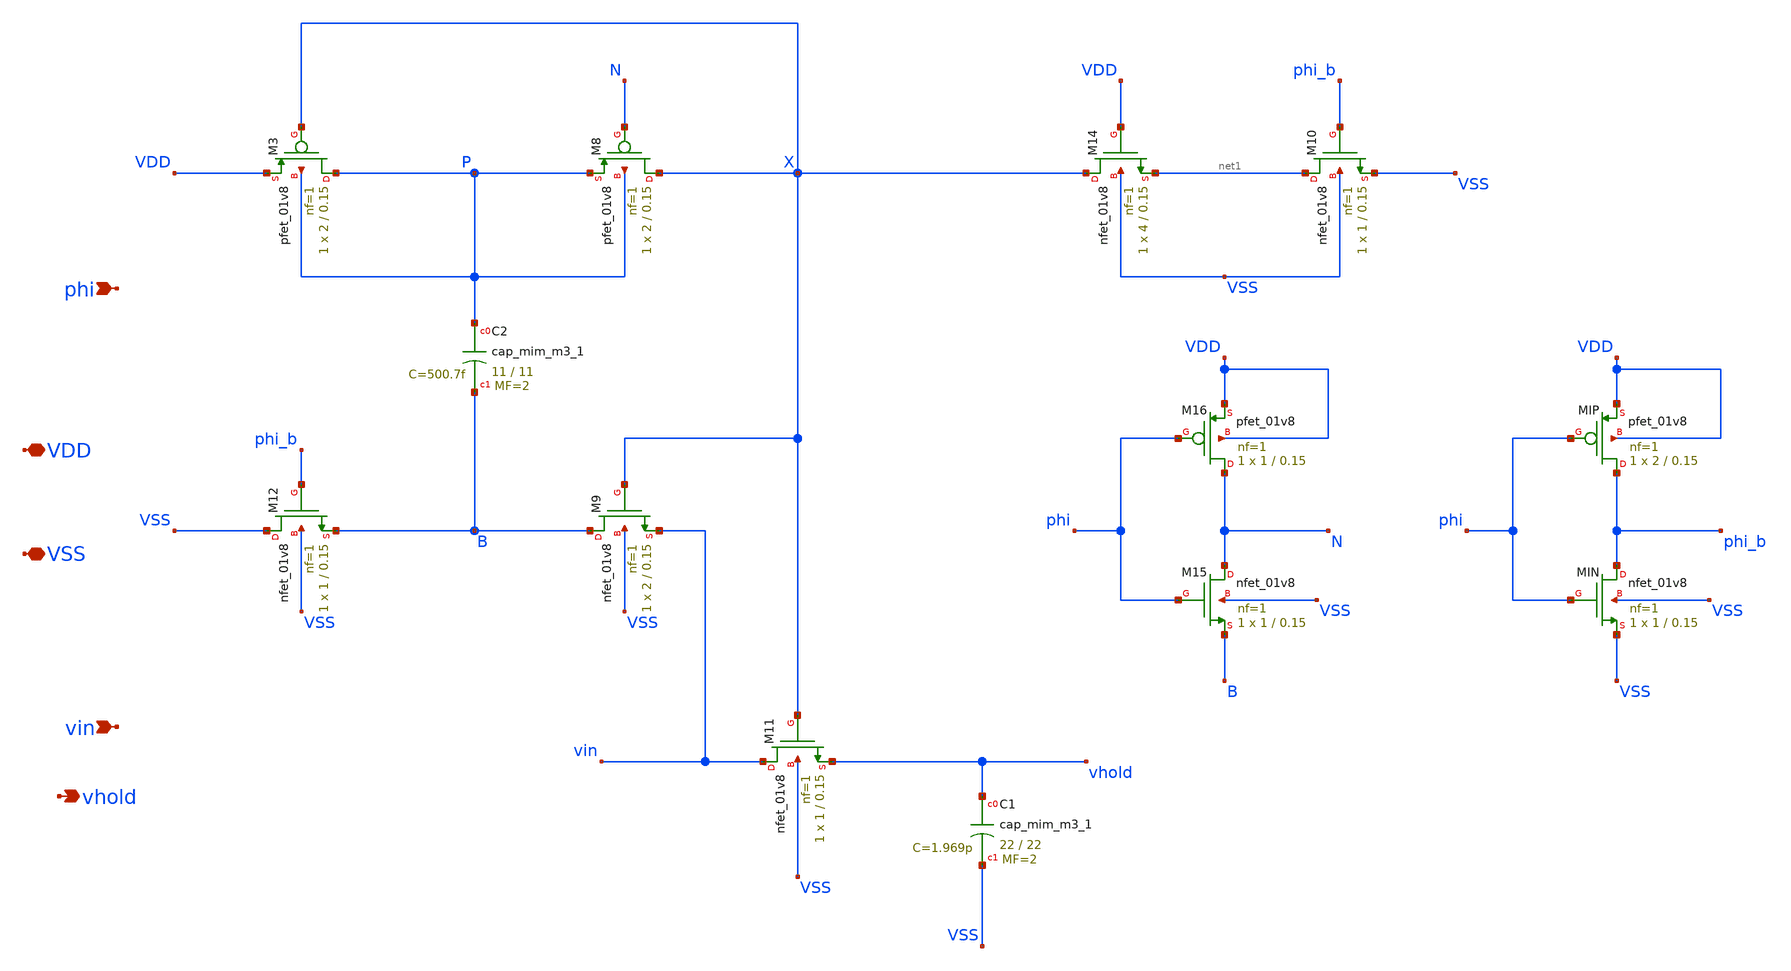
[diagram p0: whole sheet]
** sch_path: xschem/sample_hold_bootstrap.sch
**.subckt sample_hold_bootstrap VDD VSS vhold phi vin
*.iopin VDD
*.iopin VSS
*.opin vhold
*.ipin phi
*.ipin vin
XM8 X N P P sky130_fd_pr__pfet_01v8 L=0.15 W=2 nf=1 ad='int((1 + 1)/2) * 2 / 1 * 0.29' as='int((1 + 2)/2) * 2 / 1 * 0.29'
+ pd='2*int((1 + 1)/2) * (2 / 1 + 0.29)' ps='2*int((1 + 2)/2) * (2 / 1 + 0.29)' nrd='0.29 / 2 ' nrs='0.29 / 2 '
+ sa=0 sb=0 sd=0 mult=1 m=1
XM11 vin X vhold VSS sky130_fd_pr__nfet_01v8 L=0.15 W=1 nf=1 ad='int((1 + 1)/2) * 1 / 1 * 0.29' as='int((1 + 2)/2) * 1 / 1 * 0.29'
+ pd='2*int((1 + 1)/2) * (1 / 1 + 0.29)' ps='2*int((1 + 2)/2) * (1 / 1 + 0.29)' nrd='0.29 / 1 ' nrs='0.29 / 1 '
+ sa=0 sb=0 sd=0 mult=1 m=1
XC1 vhold VSS sky130_fd_pr__cap_mim_m3_1 W=22 L=22 MF=2 m=2
XC2 P B sky130_fd_pr__cap_mim_m3_1 W=11 L=11 MF=2 m=2
XM9 B X vin VSS sky130_fd_pr__nfet_01v8 L=0.15 W=2 nf=1 ad='int((1 + 1)/2) * 2 / 1 * 0.29' as='int((1 + 2)/2) * 2 / 1 * 0.29'
+ pd='2*int((1 + 1)/2) * (2 / 1 + 0.29)' ps='2*int((1 + 2)/2) * (2 / 1 + 0.29)' nrd='0.29 / 2 ' nrs='0.29 / 2 '
+ sa=0 sb=0 sd=0 mult=1 m=1
XM12 VSS phi_b B VSS sky130_fd_pr__nfet_01v8 L=0.15 W=1 nf=1 ad='int((1 + 1)/2) * 1 / 1 * 0.29' as='int((1 + 2)/2) * 1 / 1 * 0.29'
+ pd='2*int((1 + 1)/2) * (1 / 1 + 0.29)' ps='2*int((1 + 2)/2) * (1 / 1 + 0.29)' nrd='0.29 / 1 ' nrs='0.29 / 1 '
+ sa=0 sb=0 sd=0 mult=1 m=1
XM14 X VDD net1 VSS sky130_fd_pr__nfet_01v8 L=0.15 W=4 nf=1 ad='int((1 + 1)/2) * 4 / 1 * 0.29' as='int((1 + 2)/2) * 4 / 1 * 0.29'
+ pd='2*int((1 + 1)/2) * (4 / 1 + 0.29)' ps='2*int((1 + 2)/2) * (4 / 1 + 0.29)' nrd='0.29 / 4 ' nrs='0.29 / 4 '
+ sa=0 sb=0 sd=0 mult=1 m=1
XM3 P X VDD P sky130_fd_pr__pfet_01v8 L=0.15 W=2 nf=1 ad='int((1 + 1)/2) * 2 / 1 * 0.29' as='int((1 + 2)/2) * 2 / 1 * 0.29'
+ pd='2*int((1 + 1)/2) * (2 / 1 + 0.29)' ps='2*int((1 + 2)/2) * (2 / 1 + 0.29)' nrd='0.29 / 2 ' nrs='0.29 / 2 '
+ sa=0 sb=0 sd=0 mult=1 m=1
XM10 net1 phi_b VSS VSS sky130_fd_pr__nfet_01v8 L=0.15 W=1 nf=1 ad='int((1 + 1)/2) * 1 / 1 * 0.29' as='int((1 + 2)/2) * 1 / 1 * 0.29'
+ pd='2*int((1 + 1)/2) * (1 / 1 + 0.29)' ps='2*int((1 + 2)/2) * (1 / 1 + 0.29)' nrd='0.29 / 1 ' nrs='0.29 / 1 '
+ sa=0 sb=0 sd=0 mult=1 m=1
XM15 N phi B VSS sky130_fd_pr__nfet_01v8 L=0.15 W=1 nf=1 ad='int((1 + 1)/2) * 1 / 1 * 0.29' as='int((1 + 2)/2) * 1 / 1 * 0.29'
+ pd='2*int((1 + 1)/2) * (1 / 1 + 0.29)' ps='2*int((1 + 2)/2) * (1 / 1 + 0.29)' nrd='0.29 / 1 ' nrs='0.29 / 1 '
+ sa=0 sb=0 sd=0 mult=1 m=1
XM16 N phi VDD VDD sky130_fd_pr__pfet_01v8 L=0.15 W=1 nf=1 ad='int((1 + 1)/2) * 1 / 1 * 0.29' as='int((1 + 2)/2) * 1 / 1 * 0.29'
+ pd='2*int((1 + 1)/2) * (1 / 1 + 0.29)' ps='2*int((1 + 2)/2) * (1 / 1 + 0.29)' nrd='0.29 / 1 ' nrs='0.29 / 1 '
+ sa=0 sb=0 sd=0 mult=1 m=1
XMIN phi_b phi VSS VSS sky130_fd_pr__nfet_01v8 L=0.15 W=1 nf=1 ad='int((1 + 1)/2) * 1 / 1 * 0.29' as='int((1 + 2)/2) * 1 / 1 * 0.29'
+ pd='2*int((1 + 1)/2) * (1 / 1 + 0.29)' ps='2*int((1 + 2)/2) * (1 / 1 + 0.29)' nrd='0.29 / 1 ' nrs='0.29 / 1 '
+ sa=0 sb=0 sd=0 mult=1 m=1
XMIP phi_b phi VDD VDD sky130_fd_pr__pfet_01v8 L=0.15 W=2 nf=1 ad='int((1 + 1)/2) * 2 / 1 * 0.29' as='int((1 + 2)/2) * 2 / 1 * 0.29'
+ pd='2*int((1 + 1)/2) * (2 / 1 + 0.29)' ps='2*int((1 + 2)/2) * (2 / 1 + 0.29)' nrd='0.29 / 2 ' nrs='0.29 / 2 '
+ sa=0 sb=0 sd=0 mult=1 m=1
**.ends
.end
